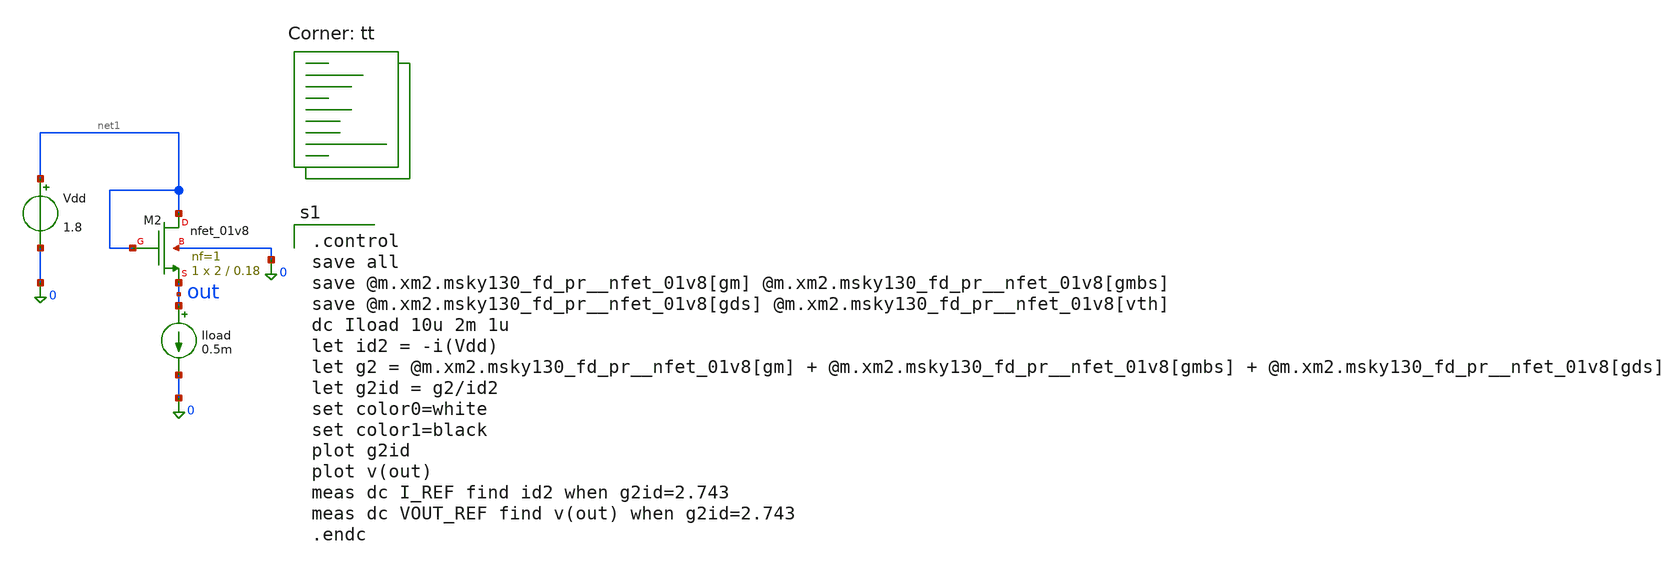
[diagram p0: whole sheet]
** sch_path: Homework 6 - Simulation on Open Source Softwares/Simulations/ex6_m2.sch
**.subckt ex6_m2
XM2 net1 net1 out 0 sky130_fd_pr__nfet_01v8 L=0.18 W=2 nf=1 ad='int((1 + 1)/2) * 2 / 1 * 0.29' as='int((1 + 2)/2) * 2 / 1 * 0.29'
+ pd='2*int((1 + 1)/2) * (2 / 1 + 0.29)' ps='2*int((1 + 2)/2) * (2 / 1 + 0.29)' nrd='0.29 / 2 ' nrs='0.29 / 2 '
+ sa=0 sb=0 sd=0 mult=1 m=1
Vdd net1 0 1.8
Iload out 0 0.5m
**** begin user architecture code

.control
save all
save @m.xm2.msky130_fd_pr__nfet_01v8[gm] @m.xm2.msky130_fd_pr__nfet_01v8[gmbs]
save @m.xm2.msky130_fd_pr__nfet_01v8[gds] @m.xm2.msky130_fd_pr__nfet_01v8[vth]
dc Iload 10u 2m 1u
let id2 = -i(Vdd)
let g2 = @m.xm2.msky130_fd_pr__nfet_01v8[gm] + @m.xm2.msky130_fd_pr__nfet_01v8[gmbs] +
+ @m.xm2.msky130_fd_pr__nfet_01v8[gds]
let g2id = g2/id2
set color0=white
set color1=black
plot g2id
plot v(out)
meas dc I_REF find id2 when g2id=2.743
meas dc VOUT_REF find v(out) when g2id=2.743
.endc

.lib $::SKYWATER_MODELS/sky130.lib.spice tt
**** end user architecture code
**.ends
.end
